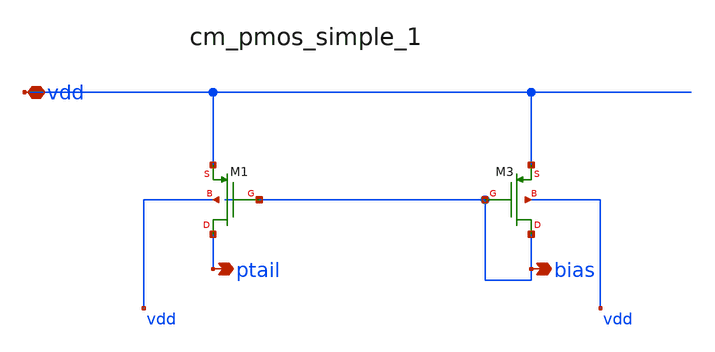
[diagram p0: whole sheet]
** sch_path: analog-db/raw/cmfb_002_5t_pmos_input/hier/blocks/cm_pmos_simple_1.sch
**.subckt cm_pmos_simple_1 vdd bias ptail
*.iopin vdd
*.opin bias
*.opin ptail
XM1 ptail bias vdd vdd sg13_lv_pmos w=x_dut_xm1_w l=x_dut_xm1_l ng=1 m=x_dut_xm1_m
XM3 bias bias vdd vdd sg13_lv_pmos w=x_dut_xm3_w l=x_dut_xm3_l ng=1 m=x_dut_xm3_m
**.ends
.end
